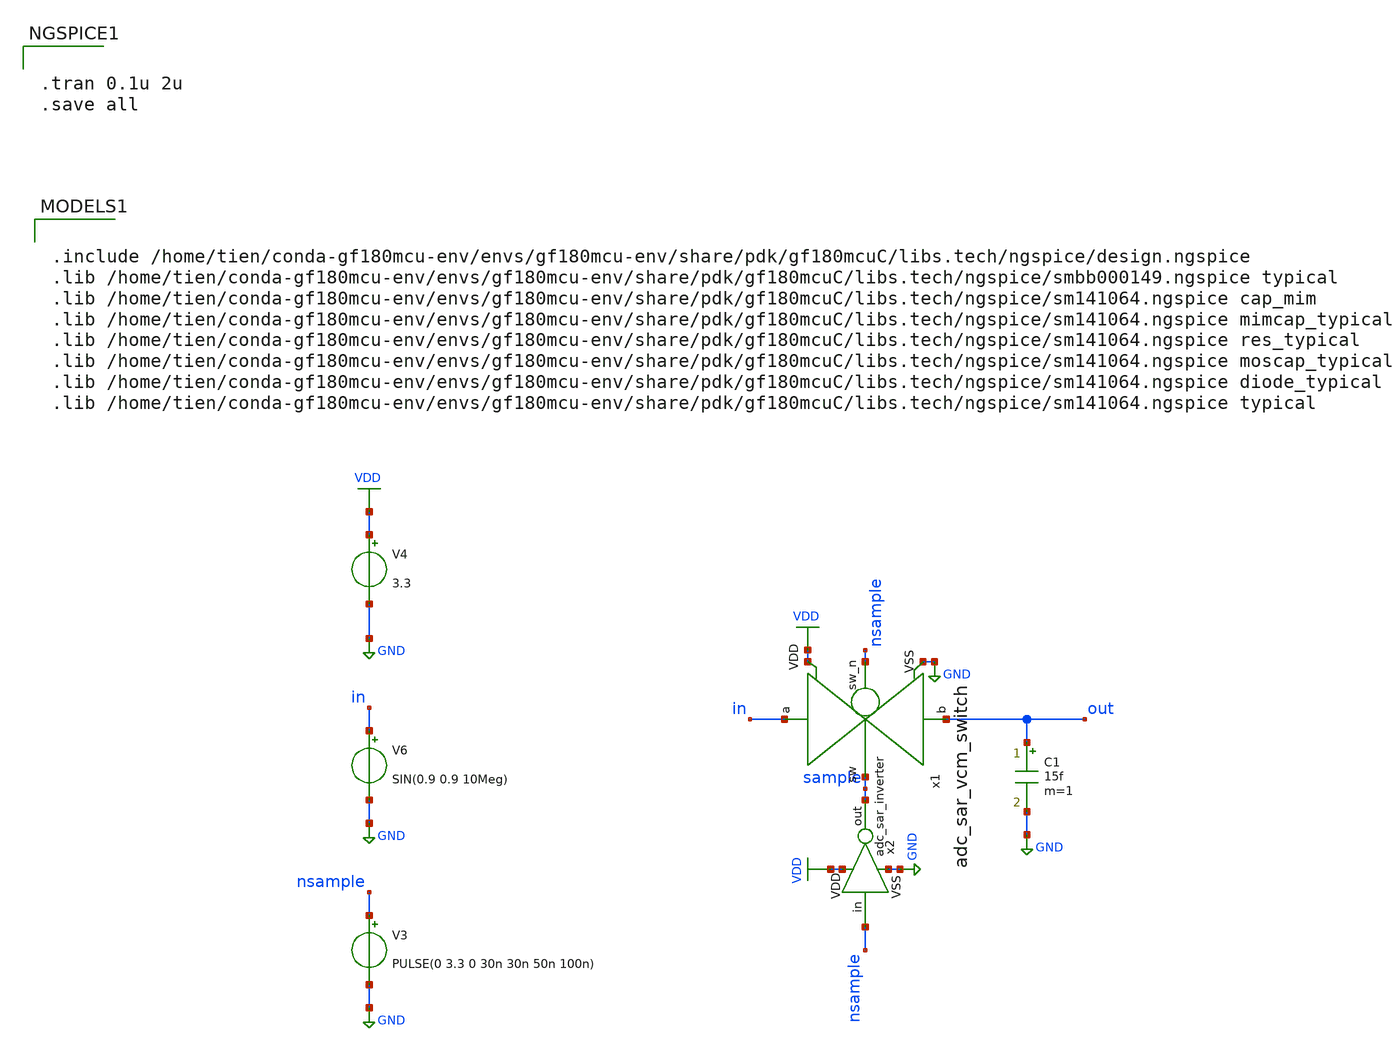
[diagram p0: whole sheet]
** sch_path: adc_sar_gate_transident_tb.sch
**.subckt adc_sar_gate_transident_tb
V3 nsample GND PULSE(0 3.3 0 30n 30n 50n 100n)
V4 VDD GND 3.3
V6 in GND SIN(0.9 0.9 10Meg)
C1 out GND 15f m=1
x1 nsample in sample out VDD GND adc_sar_vcm_switch
x2 VDD GND nsample sample adc_sar_inverter
**** begin user architecture code


.tran 0.1u 2u
.save all



.include /home/tien/conda-gf180mcu-env/envs/gf180mcu-env/share/pdk/gf180mcuC/libs.tech/ngspice/design.ngspice
.lib /home/tien/conda-gf180mcu-env/envs/gf180mcu-env/share/pdk/gf180mcuC/libs.tech/ngspice/smbb000149.ngspice typical
.lib /home/tien/conda-gf180mcu-env/envs/gf180mcu-env/share/pdk/gf180mcuC/libs.tech/ngspice/sm141064.ngspice cap_mim
.lib /home/tien/conda-gf180mcu-env/envs/gf180mcu-env/share/pdk/gf180mcuC/libs.tech/ngspice/sm141064.ngspice mimcap_typical
.lib /home/tien/conda-gf180mcu-env/envs/gf180mcu-env/share/pdk/gf180mcuC/libs.tech/ngspice/sm141064.ngspice res_typical
.lib /home/tien/conda-gf180mcu-env/envs/gf180mcu-env/share/pdk/gf180mcuC/libs.tech/ngspice/sm141064.ngspice moscap_typical
.lib /home/tien/conda-gf180mcu-env/envs/gf180mcu-env/share/pdk/gf180mcuC/libs.tech/ngspice/sm141064.ngspice diode_typical
.lib /home/tien/conda-gf180mcu-env/envs/gf180mcu-env/share/pdk/gf180mcuC/libs.tech/ngspice/sm141064.ngspice typical

**** end user architecture code
**.ends

* expanding   symbol:  adc_sar_vcm_switch.sym # of pins=6
** sym_path: adc_sar_vcm_switch.sym
** sch_path: adc_sar_vcm_switch.sch
.subckt adc_sar_vcm_switch sw_n a sw b VDD VSS
*.iopin VSS
*.iopin VDD
*.ipin sw_n
*.ipin sw
*.iopin a
*.iopin b
XM1 a sw b VSS nfet_03v3 L=0.5u W=1u nf=1 ad='int((nf+1)/2) * W/nf * 0.18u' as='int((nf+2)/2) * W/nf * 0.18u'
+ pd='2*int((nf+1)/2) * (W/nf + 0.18u)' ps='2*int((nf+2)/2) * (W/nf + 0.18u)' nrd='0.18u / W' nrs='0.18u / W'
+ sa=0 sb=0 sd=0 m=1
XM2 a sw_n b VDD pfet_03v3 L=0.5u W=1u nf=1 ad='int((nf+1)/2) * W/nf * 0.18u' as='int((nf+2)/2) * W/nf * 0.18u'
+ pd='2*int((nf+1)/2) * (W/nf + 0.18u)' ps='2*int((nf+2)/2) * (W/nf + 0.18u)' nrd='0.18u / W' nrs='0.18u / W'
+ sa=0 sb=0 sd=0 m=1
.ends


* expanding   symbol:  adc_sar_inverter.sym # of pins=4
** sym_path: adc_sar_inverter.sym
** sch_path: adc_sar_inverter.sch
.subckt adc_sar_inverter VDD VSS in out
*.iopin VDD
*.iopin VSS
*.ipin in
*.opin out
XM1 out in VSS VSS nfet_03v3 L=0.28u W=0.42u nf=1 ad='int((nf+1)/2) * W/nf * 0.18u' as='int((nf+2)/2) * W/nf * 0.18u'
+ pd='2*int((nf+1)/2) * (W/nf + 0.18u)' ps='2*int((nf+2)/2) * (W/nf + 0.18u)' nrd='0.18u / W' nrs='0.18u / W'
+ sa=0 sb=0 sd=0 m=1
XM2 out in VDD VDD pfet_03v3 L=0.28u W=0.84u nf=1 ad='int((nf+1)/2) * W/nf * 0.18u' as='int((nf+2)/2) * W/nf * 0.18u'
+ pd='2*int((nf+1)/2) * (W/nf + 0.18u)' ps='2*int((nf+2)/2) * (W/nf + 0.18u)' nrd='0.18u / W' nrs='0.18u / W'
+ sa=0 sb=0 sd=0 m=1
.ends

.GLOBAL GND
.GLOBAL VDD
.end
